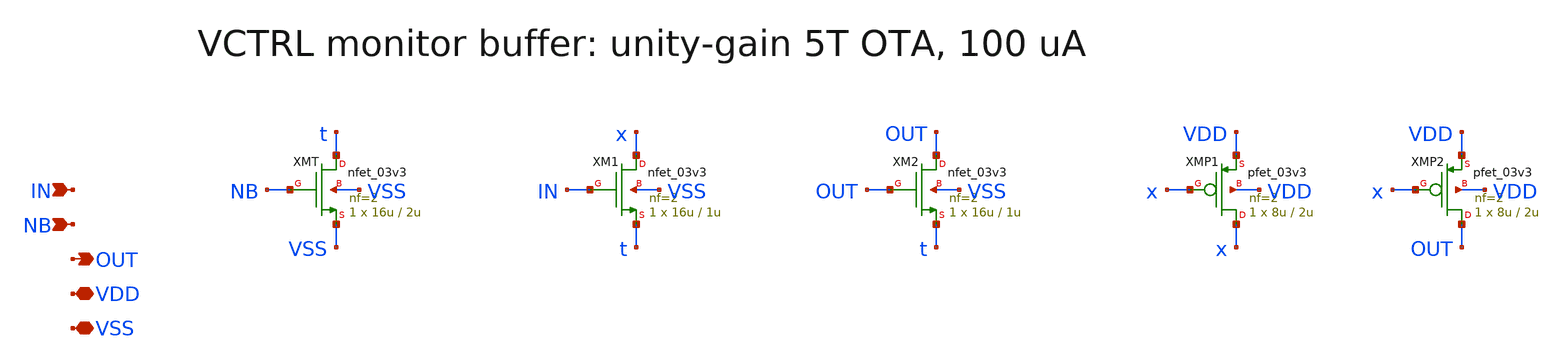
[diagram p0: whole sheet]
** sch_path: v1_claude/xschem/vmon_buf.sch
**.subckt vmon_buf IN NB OUT VDD VSS
*.ipin IN
*.ipin NB
*.opin OUT
*.iopin VDD
*.iopin VSS
XMT t NB VSS VSS nfet_03v3 L=2u W=16u nf=2 ad='int((nf+1)/2) * W/nf * 0.18u' as='int((nf+2)/2) * W/nf * 0.18u'
+ pd='2*int((nf+1)/2) * (W/nf + 0.18u)' ps='2*int((nf+2)/2) * (W/nf + 0.18u)' nrd='0.18u / W' nrs='0.18u / W'
+ sa=0 sb=0 sd=0 m=1
XM1 x IN t VSS nfet_03v3 L=1u W=16u nf=2 ad='int((nf+1)/2) * W/nf * 0.18u' as='int((nf+2)/2) * W/nf * 0.18u'
+ pd='2*int((nf+1)/2) * (W/nf + 0.18u)' ps='2*int((nf+2)/2) * (W/nf + 0.18u)' nrd='0.18u / W' nrs='0.18u / W'
+ sa=0 sb=0 sd=0 m=1
XM2 OUT OUT t VSS nfet_03v3 L=1u W=16u nf=2 ad='int((nf+1)/2) * W/nf * 0.18u' as='int((nf+2)/2) * W/nf * 0.18u'
+ pd='2*int((nf+1)/2) * (W/nf + 0.18u)' ps='2*int((nf+2)/2) * (W/nf + 0.18u)' nrd='0.18u / W' nrs='0.18u / W'
+ sa=0 sb=0 sd=0 m=1
XMP1 x x VDD VDD pfet_03v3 L=2u W=8u nf=2 ad='int((nf+1)/2) * W/nf * 0.18u' as='int((nf+2)/2) * W/nf * 0.18u'
+ pd='2*int((nf+1)/2) * (W/nf + 0.18u)' ps='2*int((nf+2)/2) * (W/nf + 0.18u)' nrd='0.18u / W' nrs='0.18u / W'
+ sa=0 sb=0 sd=0 m=1
XMP2 OUT x VDD VDD pfet_03v3 L=2u W=8u nf=2 ad='int((nf+1)/2) * W/nf * 0.18u' as='int((nf+2)/2) * W/nf * 0.18u'
+ pd='2*int((nf+1)/2) * (W/nf + 0.18u)' ps='2*int((nf+2)/2) * (W/nf + 0.18u)' nrd='0.18u / W' nrs='0.18u / W'
+ sa=0 sb=0 sd=0 m=1
**.ends
.end
